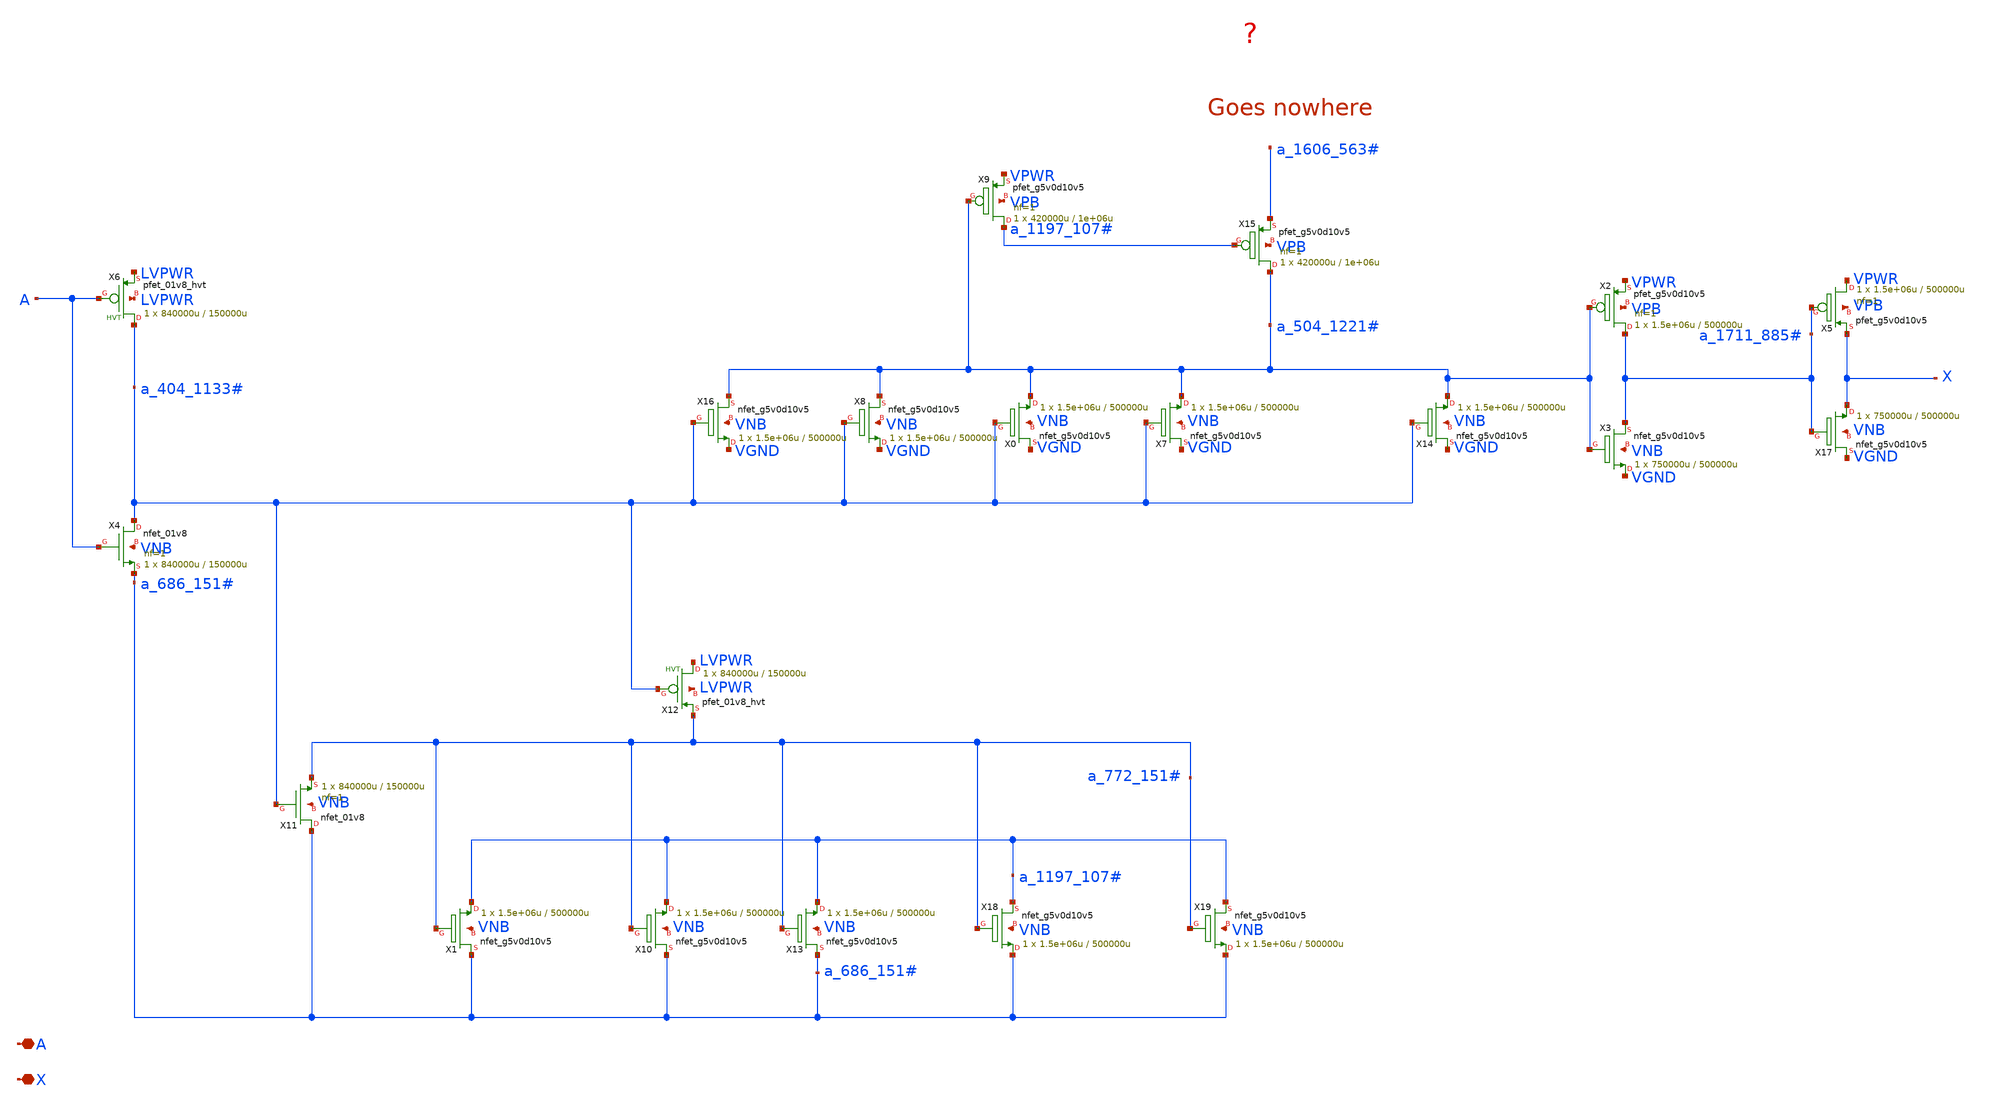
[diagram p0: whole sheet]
** sch_path: xschem_verilog_import/sky130_fd_sc_hvl__lsbuflv2hv_1_redraw.sch
**.subckt sky130_fd_sc_hvl__lsbuflv2hv_1_redraw A X
*.iopin A
*.iopin X
XX0 VGND a_404_1133# a_504_1221# VNB sky130_fd_pr__nfet_g5v0d10v5 W=1.5e+06u L=500000u ad='W * 0.29'
+ pd='W + 2 * 0.29' as='W * 0.29' ps='W + 2 * 0.29' nrd=0 nrs=0 sa=0 sb=0 sd=0 nf=1 mult=1
XX1 a_686_151# a_772_151# a_1197_107# VNB sky130_fd_pr__nfet_g5v0d10v5 W=1.5e+06u L=500000u ad='W * 0.29'
+ pd='W + 2 * 0.29' as='W * 0.29' ps='W + 2 * 0.29' nrd=0 nrs=0 sa=0 sb=0 sd=0 nf=1 mult=1
XX2 a_1711_885# a_504_1221# VPWR VPB sky130_fd_pr__pfet_g5v0d10v5 L=500000u W=1.5e+06u nf=1 ad='int((nf+1)/2) * W/nf * 0.29'
+ as='int((nf+2)/2) * W/nf * 0.29' pd='2*int((nf+1)/2) * (W/nf + 0.29)' ps='2*int((nf+2)/2) * (W/nf + 0.29)'
+ nrd='0.29 / W' nrs='0.29 / W' sa=0 sb=0 sd=0 mult=1 m=1
XX3 a_1711_885# a_504_1221# VGND VNB sky130_fd_pr__nfet_g5v0d10v5 W=750000u L=500000u ad='W * 0.29' pd='W + 2 * 0.29'
+ as='W * 0.29' ps='W + 2 * 0.29' nrd=0 nrs=0 sa=0 sb=0 sd=0 nf=1 mult=1
XX4 a_404_1133# A a_686_151# VNB sky130_fd_pr__nfet_01v8 L=150000u W=840000u nf=1 ad='int((1 + 1)/2) * 840000u / 1 * 0.29'
+ as='int((1 + 2)/2) * 840000u / 1 * 0.29' pd='2*int((1 + 1)/2) * (840000u / 1 + 0.29)' ps='2*int((1 + 2)/2) * (840000u / 1 + 0.29)'
+ nrd='0.29 / 840000u ' nrs='0.29 / 840000u ' sa=0 sb=0 sd=0 mult=1 m=1
XX5 VPWR a_1711_885# X VPB sky130_fd_pr__pfet_g5v0d10v5 L=500000u W=1.5e+06u nf=1 ad='int((nf+1)/2) * W/nf * 0.29'
+ as='int((nf+2)/2) * W/nf * 0.29' pd='2*int((nf+1)/2) * (W/nf + 0.29)' ps='2*int((nf+2)/2) * (W/nf + 0.29)'
+ nrd='0.29 / W' nrs='0.29 / W' sa=0 sb=0 sd=0 mult=1 m=1
XX6 a_404_1133# A LVPWR LVPWR sky130_fd_pr__pfet_01v8_hvt W=840000u L=150000u ad='W * 0.29' pd='W + 2 * 0.29'
+ as='W * 0.29' ps='W + 2 * 0.29' nrd=0 nrs=0 sa=0 sb=0 sd=0 nf=1 mult=1
XX7 VGND a_404_1133# a_504_1221# VNB sky130_fd_pr__nfet_g5v0d10v5 W=1.5e+06u L=500000u ad='W * 0.29'
+ pd='W + 2 * 0.29' as='W * 0.29' ps='W + 2 * 0.29' nrd=0 nrs=0 sa=0 sb=0 sd=0 nf=1 mult=1
XX8 a_504_1221# a_404_1133# VGND VNB sky130_fd_pr__nfet_g5v0d10v5 W=1.5e+06u L=500000u ad='W * 0.29'
+ pd='W + 2 * 0.29' as='W * 0.29' ps='W + 2 * 0.29' nrd=0 nrs=0 sa=0 sb=0 sd=0 nf=1 mult=1
XX9 a_1197_107# a_504_1221# VPWR VPB sky130_fd_pr__pfet_g5v0d10v5 L=1e+06u W=420000u nf=1 ad='int((nf+1)/2) * W/nf * 0.29'
+ as='int((nf+2)/2) * W/nf * 0.29' pd='2*int((nf+1)/2) * (W/nf + 0.29)' ps='2*int((nf+2)/2) * (W/nf + 0.29)'
+ nrd='0.29 / W' nrs='0.29 / W' sa=0 sb=0 sd=0 mult=1 m=1
XX10 a_686_151# a_772_151# a_1197_107# VNB sky130_fd_pr__nfet_g5v0d10v5 W=1.5e+06u L=500000u ad='W * 0.29'
+ pd='W + 2 * 0.29' as='W * 0.29' ps='W + 2 * 0.29' nrd=0 nrs=0 sa=0 sb=0 sd=0 nf=1 mult=1
XX11 a_686_151# a_404_1133# a_772_151# VNB sky130_fd_pr__nfet_01v8 L=150000u W=840000u nf=1 ad='int((1 + 1)/2) * 840000u / 1 * 0.29'
+ as='int((1 + 2)/2) * 840000u / 1 * 0.29' pd='2*int((1 + 1)/2) * (840000u / 1 + 0.29)' ps='2*int((1 + 2)/2) * (840000u / 1 + 0.29)'
+ nrd='0.29 / 840000u ' nrs='0.29 / 840000u ' sa=0 sb=0 sd=0 mult=1 m=1
XX12 LVPWR a_404_1133# a_772_151# LVPWR sky130_fd_pr__pfet_01v8_hvt W=840000u L=150000u ad='W * 0.29'
+ pd='W + 2 * 0.29' as='W * 0.29' ps='W + 2 * 0.29' nrd=0 nrs=0 sa=0 sb=0 sd=0 nf=1 mult=1
XX13 a_686_151# a_772_151# a_1197_107# VNB sky130_fd_pr__nfet_g5v0d10v5 W=1.5e+06u L=500000u ad='W * 0.29'
+ pd='W + 2 * 0.29' as='W * 0.29' ps='W + 2 * 0.29' nrd=0 nrs=0 sa=0 sb=0 sd=0 nf=1 mult=1
XX14 VGND a_404_1133# a_504_1221# VNB sky130_fd_pr__nfet_g5v0d10v5 W=1.5e+06u L=500000u ad='W * 0.29'
+ pd='W + 2 * 0.29' as='W * 0.29' ps='W + 2 * 0.29' nrd=0 nrs=0 sa=0 sb=0 sd=0 nf=1 mult=1
XX15 a_504_1221# a_1197_107# a_1606_563# VPB sky130_fd_pr__pfet_g5v0d10v5 L=1e+06u W=420000u nf=1 ad='int((nf+1)/2) * W/nf * 0.29'
+ as='int((nf+2)/2) * W/nf * 0.29' pd='2*int((nf+1)/2) * (W/nf + 0.29)' ps='2*int((nf+2)/2) * (W/nf + 0.29)'
+ nrd='0.29 / W' nrs='0.29 / W' sa=0 sb=0 sd=0 mult=1 m=1
XX16 a_504_1221# a_404_1133# VGND VNB sky130_fd_pr__nfet_g5v0d10v5 W=1.5e+06u L=500000u ad='W * 0.29'
+ pd='W + 2 * 0.29' as='W * 0.29' ps='W + 2 * 0.29' nrd=0 nrs=0 sa=0 sb=0 sd=0 nf=1 mult=1
XX17 VGND a_1711_885# X VNB sky130_fd_pr__nfet_g5v0d10v5 W=750000u L=500000u ad='W * 0.29' pd='W + 2 * 0.29'
+ as='W * 0.29' ps='W + 2 * 0.29' nrd=0 nrs=0 sa=0 sb=0 sd=0 nf=1 mult=1
XX18 a_1197_107# a_772_151# a_686_151# VNB sky130_fd_pr__nfet_g5v0d10v5 W=1.5e+06u L=500000u ad='W * 0.29'
+ pd='W + 2 * 0.29' as='W * 0.29' ps='W + 2 * 0.29' nrd=0 nrs=0 sa=0 sb=0 sd=0 nf=1 mult=1
XX19 a_1197_107# a_772_151# a_686_151# VNB sky130_fd_pr__nfet_g5v0d10v5 W=1.5e+06u L=500000u ad='W * 0.29'
+ pd='W + 2 * 0.29' as='W * 0.29' ps='W + 2 * 0.29' nrd=0 nrs=0 sa=0 sb=0 sd=0 nf=1 mult=1
**.ends
.end
